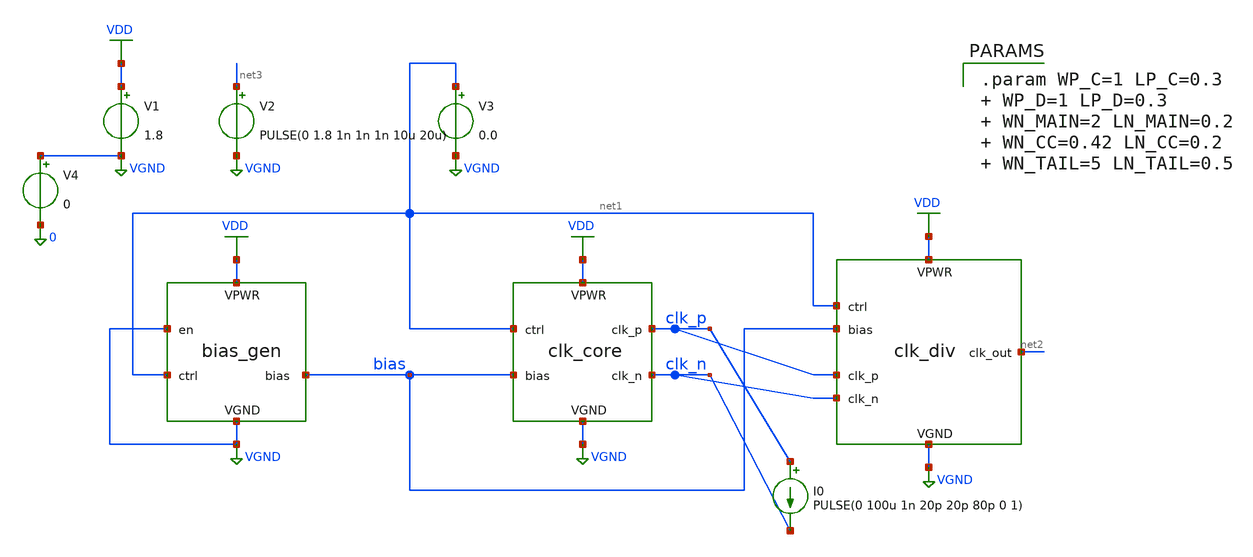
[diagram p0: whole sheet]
** sch_path: simple_vco/v1/tb_proto.sch
**.subckt tb_proto
x1 VDD VGND VGND net1 bias bias_gen
x2 VDD VGND net1 bias clk_p clk_n clk_core
x3 VDD VGND net1 bias clk_p clk_n net2 clk_div
V1 VDD VGND 1.8
V2 net3 VGND PULSE(0 1.8 1n 1n 1n 10u 20u)
V3 net1 VGND 0.0
V4 VGND 0 0
I0 clk_p clk_n PULSE(0 100u 1n 20p 20p 80p 0 1)
**** begin user architecture code


** opencircuitdesign pdks install

.lib $::SKYWATER_MODELS/sky130.lib.spice tt

.include $::SKYWATER_STDCELLS/sky130_fd_sc_hd.spice





.param mc_mm_switch=0
*.option savecurrents
.control

*save all

tran 5p 50n
*plot CLK_OUT CLK_P CLK_N
*plot diff_out
*plot bias

quit 0

.endc

.end




.param WP_C=1 LP_C=0.3  WP_D=1 LP_D=0.3  WN_MAIN=2 LN_MAIN=0.2  WN_CC=0.42 LN_CC=0.2  WN_TAIL=5
+ LN_TAIL=0.5




* 1. Create a continuous differential signal
*B_diff_clk diff_out 0 V=V(clk_p) - V(clk_n)

* 2. Frequency Measurement
* (Wait for the 30th crossing to ensure any startup jitter is gone)
*.meas tran t_start TRIG V(diff_out) VAL=0 RISE=30
*.meas tran t_end   TRIG V(diff_out) VAL=0 RISE=41
*.meas tran period  PARAM='t_end - t_start'
*.meas tran freq    PARAM='1/period'

* 3. Amplitude / Robustness Measurement
* (Measure the peak differential voltage during that exact period)
*.meas tran v_peak MAX V(diff_out) FROM=t_start TO=t_end
*.meas tran v_pp PP V(diff_out) from=30n to=40n


* 1. Create a continuous differential signal
B_diff_clk diff_out 0 V=V(clk_p) - V(clk_n)

* 2. Frequency Measurement
* (Using WHEN to grab exact timestamps)
.meas tran t_start WHEN V(diff_out)=0 RISE=30
.meas tran t_end   WHEN V(diff_out)=0 RISE=41

* (Divide by 11 because RISE 30 to 41 is 11 cycles)
.meas tran period  PARAM='(t_end - t_start) / 11'
.meas tran freq    PARAM='1 / period'

* 3. Amplitude / Robustness Measurement
* (Your static window Peak-to-Peak approach)
.meas tran v_pp PP V(diff_out) FROM=30n TO=40n


**** end user architecture code
**.ends

* expanding   symbol:  bias_gen.sym # of pins=5
** sym_path: simple_vco/v1/bias_gen.sym
** sch_path: simple_vco/v1/bias_gen.sch
.subckt bias_gen VPWR VGND en ctrl bias_out
*.iopin VPWR
*.iopin VGND
*.ipin en
*.ipin ctrl
*.opin bias_out
XM8 net5 net5 VPWR VPWR sky130_fd_pr__pfet_01v8 L=0.3 W=5 nf=1 ad='int((1 + 1)/2) * 5 / 1 * 0.29' as='int((1 + 2)/2) * 5 / 1 * 0.29'
+ pd='2*int((1 + 1)/2) * (5 / 1 + 0.29)' ps='2*int((1 + 2)/2) * (5 / 1 + 0.29)' nrd='0.29 / 5 ' nrs='0.29 / 5 '
+ sa=0 sb=0 sd=0 mult=1 m=1
XM7 bias_out ctrl net3 VPWR sky130_fd_pr__pfet_01v8 L=0.3 W=2 nf=1 ad='int((1 + 1)/2) * 2 / 1 * 0.29'
+ as='int((1 + 2)/2) * 2 / 1 * 0.29' pd='2*int((1 + 1)/2) * (2 / 1 + 0.29)' ps='2*int((1 + 2)/2) * (2 / 1 + 0.29)'
+ nrd='0.29 / 2 ' nrs='0.29 / 2 ' sa=0 sb=0 sd=0 mult=1 m=1
XM6 net4 net1 net3 VPWR sky130_fd_pr__pfet_01v8 L=0.3 W=2 nf=1 ad='int((1 + 1)/2) * 2 / 1 * 0.29' as='int((1 + 2)/2) * 2 / 1 * 0.29'
+ pd='2*int((1 + 1)/2) * (2 / 1 + 0.29)' ps='2*int((1 + 2)/2) * (2 / 1 + 0.29)' nrd='0.29 / 2 ' nrs='0.29 / 2 '
+ sa=0 sb=0 sd=0 mult=1 m=1
XM3 net1 ctrl VPWR VPWR sky130_fd_pr__pfet_01v8 L=LP_C W=WP_C nf=1 ad='int((1 + 1)/2) * WP_C / 1 * 0.29'
+ as='int((1 + 2)/2) * WP_C / 1 * 0.29' pd='2*int((1 + 1)/2) * (WP_C / 1 + 0.29)' ps='2*int((1 + 2)/2) * (WP_C / 1 + 0.29)'
+ nrd='0.29 / WP_C ' nrs='0.29 / WP_C ' sa=0 sb=0 sd=0 mult=1 m=1
XM1 net1 net1 VPWR VPWR sky130_fd_pr__pfet_01v8 L=LP_D W=WP_D nf=1 ad='int((1 + 1)/2) * WP_D / 1 * 0.29'
+ as='int((1 + 2)/2) * WP_D / 1 * 0.29' pd='2*int((1 + 1)/2) * (WP_D / 1 + 0.29)' ps='2*int((1 + 2)/2) * (WP_D / 1 + 0.29)'
+ nrd='0.29 / WP_D ' nrs='0.29 / WP_D ' sa=0 sb=0 sd=0 mult=1 m=1
XM5 net3 net5 VPWR VPWR sky130_fd_pr__pfet_01v8 L=0.3 W=5 nf=1 ad='int((1 + 1)/2) * 5 / 1 * 0.29' as='int((1 + 2)/2) * 5 / 1 * 0.29'
+ pd='2*int((1 + 1)/2) * (5 / 1 + 0.29)' ps='2*int((1 + 2)/2) * (5 / 1 + 0.29)' nrd='0.29 / 5 ' nrs='0.29 / 5 '
+ sa=0 sb=0 sd=0 mult=1 m=1
XM9 bias_out net4 VGND VGND sky130_fd_pr__nfet_01v8 L=0.5 W=5 nf=1 ad='int((1 + 1)/2) * 5 / 1 * 0.29'
+ as='int((1 + 2)/2) * 5 / 1 * 0.29' pd='2*int((1 + 1)/2) * (5 / 1 + 0.29)' ps='2*int((1 + 2)/2) * (5 / 1 + 0.29)'
+ nrd='0.29 / 5 ' nrs='0.29 / 5 ' sa=0 sb=0 sd=0 mult=1 m=1
XM10 net4 net4 VGND VGND sky130_fd_pr__nfet_01v8 L=0.5 W=5 nf=1 ad='int((1 + 1)/2) * 5 / 1 * 0.29' as='int((1 + 2)/2) * 5 / 1 * 0.29'
+ pd='2*int((1 + 1)/2) * (5 / 1 + 0.29)' ps='2*int((1 + 2)/2) * (5 / 1 + 0.29)' nrd='0.29 / 5 ' nrs='0.29 / 5 '
+ sa=0 sb=0 sd=0 mult=1 m=1
XM11 net5 VPWR net6 VGND sky130_fd_pr__nfet_01v8 L=0.2 W=2 nf=1 ad='int((1 + 1)/2) * 2 / 1 * 0.29' as='int((1 + 2)/2) * 2 / 1 * 0.29'
+ pd='2*int((1 + 1)/2) * (2 / 1 + 0.29)' ps='2*int((1 + 2)/2) * (2 / 1 + 0.29)' nrd='0.29 / 2 ' nrs='0.29 / 2 '
+ sa=0 sb=0 sd=0 mult=1 m=1
XM12 net6 bias_out VGND VGND sky130_fd_pr__nfet_01v8 L=0.5 W=5 nf=1 ad='int((1 + 1)/2) * 5 / 1 * 0.29'
+ as='int((1 + 2)/2) * 5 / 1 * 0.29' pd='2*int((1 + 1)/2) * (5 / 1 + 0.29)' ps='2*int((1 + 2)/2) * (5 / 1 + 0.29)'
+ nrd='0.29 / 5 ' nrs='0.29 / 5 ' sa=0 sb=0 sd=0 mult=1 m=1
XM13 net6 net7 VGND VGND sky130_fd_pr__nfet_01v8 L=0.15 W=5 nf=1 ad='int((1 + 1)/2) * 5 / 1 * 0.29' as='int((1 + 2)/2) * 5 / 1 * 0.29'
+ pd='2*int((1 + 1)/2) * (5 / 1 + 0.29)' ps='2*int((1 + 2)/2) * (5 / 1 + 0.29)' nrd='0.29 / 5 ' nrs='0.29 / 5 '
+ sa=0 sb=0 sd=0 mult=1 m=1
XM14 net7 net8 VPWR VPWR sky130_fd_pr__pfet_01v8 L=0.15 W=1 nf=1 ad='int((1 + 1)/2) * 1 / 1 * 0.29' as='int((1 + 2)/2) * 1 / 1 * 0.29'
+ pd='2*int((1 + 1)/2) * (1 / 1 + 0.29)' ps='2*int((1 + 2)/2) * (1 / 1 + 0.29)' nrd='0.29 / 1 ' nrs='0.29 / 1 '
+ sa=0 sb=0 sd=0 mult=1 m=1
XM15 net7 net8 VGND VGND sky130_fd_pr__nfet_01v8 L=0.15 W=1 nf=1 ad='int((1 + 1)/2) * 1 / 1 * 0.29' as='int((1 + 2)/2) * 1 / 1 * 0.29'
+ pd='2*int((1 + 1)/2) * (1 / 1 + 0.29)' ps='2*int((1 + 2)/2) * (1 / 1 + 0.29)' nrd='0.29 / 1 ' nrs='0.29 / 1 '
+ sa=0 sb=0 sd=0 mult=1 m=1
XM16 net8 net9 VPWR VPWR sky130_fd_pr__pfet_01v8 L=0.15 W=1 nf=1 ad='int((1 + 1)/2) * 1 / 1 * 0.29' as='int((1 + 2)/2) * 1 / 1 * 0.29'
+ pd='2*int((1 + 1)/2) * (1 / 1 + 0.29)' ps='2*int((1 + 2)/2) * (1 / 1 + 0.29)' nrd='0.29 / 1 ' nrs='0.29 / 1 '
+ sa=0 sb=0 sd=0 mult=1 m=1
XM17 net8 net9 VGND VGND sky130_fd_pr__nfet_01v8 L=0.15 W=1 nf=1 ad='int((1 + 1)/2) * 1 / 1 * 0.29' as='int((1 + 2)/2) * 1 / 1 * 0.29'
+ pd='2*int((1 + 1)/2) * (1 / 1 + 0.29)' ps='2*int((1 + 2)/2) * (1 / 1 + 0.29)' nrd='0.29 / 1 ' nrs='0.29 / 1 '
+ sa=0 sb=0 sd=0 mult=1 m=1
XM19 net9 bias_out VGND VGND sky130_fd_pr__nfet_01v8 L=0.15 W=1 nf=1 ad='int((1 + 1)/2) * 1 / 1 * 0.29'
+ as='int((1 + 2)/2) * 1 / 1 * 0.29' pd='2*int((1 + 1)/2) * (1 / 1 + 0.29)' ps='2*int((1 + 2)/2) * (1 / 1 + 0.29)'
+ nrd='0.29 / 1 ' nrs='0.29 / 1 ' sa=0 sb=0 sd=0 mult=1 m=1
XM18 net9 en VPWR VPWR sky130_fd_pr__pfet_01v8_hvt L=8 W=0.42 nf=1 ad='int((1 + 1)/2) * 0.42 / 1 * 0.29'
+ as='int((1 + 2)/2) * 0.42 / 1 * 0.29' pd='2*int((1 + 1)/2) * (0.42 / 1 + 0.29)' ps='2*int((1 + 2)/2) * (0.42 / 1 + 0.29)'
+ nrd='0.29 / 0.42 ' nrs='0.29 / 0.42 ' sa=0 sb=0 sd=0 mult=1 m=1
XM20 bias_out en VGND VGND sky130_fd_pr__nfet_01v8 L=0.15 W=0.42 nf=1 ad='int((1 + 1)/2) * 0.42 / 1 * 0.29'
+ as='int((1 + 2)/2) * 0.42 / 1 * 0.29' pd='2*int((1 + 1)/2) * (0.42 / 1 + 0.29)' ps='2*int((1 + 2)/2) * (0.42 / 1 + 0.29)'
+ nrd='0.29 / 0.42 ' nrs='0.29 / 0.42 ' sa=0 sb=0 sd=0 mult=1 m=1
XM21 net9 en VGND VGND sky130_fd_pr__nfet_01v8 L=0.15 W=0.42 nf=1 ad='int((1 + 1)/2) * 0.42 / 1 * 0.29'
+ as='int((1 + 2)/2) * 0.42 / 1 * 0.29' pd='2*int((1 + 1)/2) * (0.42 / 1 + 0.29)' ps='2*int((1 + 2)/2) * (0.42 / 1 + 0.29)'
+ nrd='0.29 / 0.42 ' nrs='0.29 / 0.42 ' sa=0 sb=0 sd=0 mult=1 m=1
XM4 net2 bias_out VGND VGND sky130_fd_pr__nfet_01v8 L=LN_TAIL W=WN_TAIL nf=1 ad='int((1 + 1)/2) * WN_TAIL / 1 * 0.29'
+ as='int((1 + 2)/2) * WN_TAIL / 1 * 0.29' pd='2*int((1 + 1)/2) * (WN_TAIL / 1 + 0.29)' ps='2*int((1 + 2)/2) * (WN_TAIL / 1 + 0.29)'
+ nrd='0.29 / WN_TAIL ' nrs='0.29 / WN_TAIL ' sa=0 sb=0 sd=0 mult=1 m=1
XM2 net1 VPWR net2 VGND sky130_fd_pr__nfet_01v8 L=LN_MAIN W=WN_MAIN nf=1 ad='int((1 + 1)/2) * WN_MAIN / 1 * 0.29'
+ as='int((1 + 2)/2) * WN_MAIN / 1 * 0.29' pd='2*int((1 + 1)/2) * (WN_MAIN / 1 + 0.29)' ps='2*int((1 + 2)/2) * (WN_MAIN / 1 + 0.29)'
+ nrd='0.29 / WN_MAIN ' nrs='0.29 / WN_MAIN ' sa=0 sb=0 sd=0 mult=1 m=1
.ends


* expanding   symbol:  clk_core.sym # of pins=6
** sym_path: simple_vco/v1/clk_core.sym
** sch_path: simple_vco/v1/clk_core.sch
.subckt clk_core VPWR VGND ctrl bias_in clk_p clk_n
*.iopin VPWR
*.iopin VGND
*.ipin ctrl
*.ipin bias_in
*.opin clk_p
*.opin clk_n
XM3 clk_p ctrl VPWR VPWR sky130_fd_pr__pfet_01v8 L=LP_C W=WP_C nf=1 ad='int((1 + 1)/2) * WP_C / 1 * 0.29'
+ as='int((1 + 2)/2) * WP_C / 1 * 0.29' pd='2*int((1 + 1)/2) * (WP_C / 1 + 0.29)' ps='2*int((1 + 2)/2) * (WP_C / 1 + 0.29)'
+ nrd='0.29 / WP_C ' nrs='0.29 / WP_C ' sa=0 sb=0 sd=0 mult=1 m=1
XM1 clk_p clk_p VPWR VPWR sky130_fd_pr__pfet_01v8 L=LP_D W=WP_D nf=1 ad='int((1 + 1)/2) * WP_D / 1 * 0.29'
+ as='int((1 + 2)/2) * WP_D / 1 * 0.29' pd='2*int((1 + 1)/2) * (WP_D / 1 + 0.29)' ps='2*int((1 + 2)/2) * (WP_D / 1 + 0.29)'
+ nrd='0.29 / WP_D ' nrs='0.29 / WP_D ' sa=0 sb=0 sd=0 mult=1 m=1
XM4 net1 bias_in VGND VGND sky130_fd_pr__nfet_01v8 L=LN_TAIL W=WN_TAIL nf=1 ad='int((1 + 1)/2) * WN_TAIL / 1 * 0.29'
+ as='int((1 + 2)/2) * WN_TAIL / 1 * 0.29' pd='2*int((1 + 1)/2) * (WN_TAIL / 1 + 0.29)' ps='2*int((1 + 2)/2) * (WN_TAIL / 1 + 0.29)'
+ nrd='0.29 / WN_TAIL ' nrs='0.29 / WN_TAIL ' sa=0 sb=0 sd=0 mult=1 m=1
XM2 clk_p clk_2_p net1 VGND sky130_fd_pr__nfet_01v8 L=LN_MAIN W=WN_MAIN nf=1 ad='int((1 + 1)/2) * WN_MAIN / 1 * 0.29'
+ as='int((1 + 2)/2) * WN_MAIN / 1 * 0.29' pd='2*int((1 + 1)/2) * (WN_MAIN / 1 + 0.29)' ps='2*int((1 + 2)/2) * (WN_MAIN / 1 + 0.29)'
+ nrd='0.29 / WN_MAIN ' nrs='0.29 / WN_MAIN ' sa=0 sb=0 sd=0 mult=1 m=1
XM5 clk_n ctrl VPWR VPWR sky130_fd_pr__pfet_01v8 L=LP_C W=WP_C nf=1 ad='int((1 + 1)/2) * WP_C / 1 * 0.29'
+ as='int((1 + 2)/2) * WP_C / 1 * 0.29' pd='2*int((1 + 1)/2) * (WP_C / 1 + 0.29)' ps='2*int((1 + 2)/2) * (WP_C / 1 + 0.29)'
+ nrd='0.29 / WP_C ' nrs='0.29 / WP_C ' sa=0 sb=0 sd=0 mult=1 m=1
XM6 clk_n clk_n VPWR VPWR sky130_fd_pr__pfet_01v8 L=LP_D W=WP_D nf=1 ad='int((1 + 1)/2) * WP_D / 1 * 0.29'
+ as='int((1 + 2)/2) * WP_D / 1 * 0.29' pd='2*int((1 + 1)/2) * (WP_D / 1 + 0.29)' ps='2*int((1 + 2)/2) * (WP_D / 1 + 0.29)'
+ nrd='0.29 / WP_D ' nrs='0.29 / WP_D ' sa=0 sb=0 sd=0 mult=1 m=1
XM8 clk_n clk_2_n net1 VGND sky130_fd_pr__nfet_01v8 L=LN_MAIN W=WN_MAIN nf=1 ad='int((1 + 1)/2) * WN_MAIN / 1 * 0.29'
+ as='int((1 + 2)/2) * WN_MAIN / 1 * 0.29' pd='2*int((1 + 1)/2) * (WN_MAIN / 1 + 0.29)' ps='2*int((1 + 2)/2) * (WN_MAIN / 1 + 0.29)'
+ nrd='0.29 / WN_MAIN ' nrs='0.29 / WN_MAIN ' sa=0 sb=0 sd=0 mult=1 m=1
XM7 clk_n clk_p net1 VGND sky130_fd_pr__nfet_01v8 L=LN_CC W=WN_CC nf=1 ad='int((1 + 1)/2) * WN_CC / 1 * 0.29'
+ as='int((1 + 2)/2) * WN_CC / 1 * 0.29' pd='2*int((1 + 1)/2) * (WN_CC / 1 + 0.29)' ps='2*int((1 + 2)/2) * (WN_CC / 1 + 0.29)'
+ nrd='0.29 / WN_CC ' nrs='0.29 / WN_CC ' sa=0 sb=0 sd=0 mult=1 m=1
XM9 clk_p clk_n net1 VGND sky130_fd_pr__nfet_01v8 L=LN_CC W=WN_CC nf=1 ad='int((1 + 1)/2) * WN_CC / 1 * 0.29'
+ as='int((1 + 2)/2) * WN_CC / 1 * 0.29' pd='2*int((1 + 1)/2) * (WN_CC / 1 + 0.29)' ps='2*int((1 + 2)/2) * (WN_CC / 1 + 0.29)'
+ nrd='0.29 / WN_CC ' nrs='0.29 / WN_CC ' sa=0 sb=0 sd=0 mult=1 m=1
XM10 clk_2_n ctrl VPWR VPWR sky130_fd_pr__pfet_01v8 L=LP_C W=WP_C nf=1 ad='int((1 + 1)/2) * WP_C / 1 * 0.29'
+ as='int((1 + 2)/2) * WP_C / 1 * 0.29' pd='2*int((1 + 1)/2) * (WP_C / 1 + 0.29)' ps='2*int((1 + 2)/2) * (WP_C / 1 + 0.29)'
+ nrd='0.29 / WP_C ' nrs='0.29 / WP_C ' sa=0 sb=0 sd=0 mult=1 m=1
XM11 clk_2_n clk_2_n VPWR VPWR sky130_fd_pr__pfet_01v8 L=LP_D W=WP_D nf=1 ad='int((1 + 1)/2) * WP_D / 1 * 0.29'
+ as='int((1 + 2)/2) * WP_D / 1 * 0.29' pd='2*int((1 + 1)/2) * (WP_D / 1 + 0.29)' ps='2*int((1 + 2)/2) * (WP_D / 1 + 0.29)'
+ nrd='0.29 / WP_D ' nrs='0.29 / WP_D ' sa=0 sb=0 sd=0 mult=1 m=1
XM12 net2 bias_in VGND VGND sky130_fd_pr__nfet_01v8 L=LN_TAIL W=WN_TAIL nf=1 ad='int((1 + 1)/2) * WN_TAIL / 1 * 0.29'
+ as='int((1 + 2)/2) * WN_TAIL / 1 * 0.29' pd='2*int((1 + 1)/2) * (WN_TAIL / 1 + 0.29)' ps='2*int((1 + 2)/2) * (WN_TAIL / 1 + 0.29)'
+ nrd='0.29 / WN_TAIL ' nrs='0.29 / WN_TAIL ' sa=0 sb=0 sd=0 mult=1 m=1
XM13 clk_2_n clk_p net2 VGND sky130_fd_pr__nfet_01v8 L=LN_MAIN W=WN_MAIN nf=1 ad='int((1 + 1)/2) * WN_MAIN / 1 * 0.29'
+ as='int((1 + 2)/2) * WN_MAIN / 1 * 0.29' pd='2*int((1 + 1)/2) * (WN_MAIN / 1 + 0.29)' ps='2*int((1 + 2)/2) * (WN_MAIN / 1 + 0.29)'
+ nrd='0.29 / WN_MAIN ' nrs='0.29 / WN_MAIN ' sa=0 sb=0 sd=0 mult=1 m=1
XM14 clk_2_p ctrl VPWR VPWR sky130_fd_pr__pfet_01v8 L=LP_C W=WP_C nf=1 ad='int((1 + 1)/2) * WP_C / 1 * 0.29'
+ as='int((1 + 2)/2) * WP_C / 1 * 0.29' pd='2*int((1 + 1)/2) * (WP_C / 1 + 0.29)' ps='2*int((1 + 2)/2) * (WP_C / 1 + 0.29)'
+ nrd='0.29 / WP_C ' nrs='0.29 / WP_C ' sa=0 sb=0 sd=0 mult=1 m=1
XM15 clk_2_p clk_2_p VPWR VPWR sky130_fd_pr__pfet_01v8 L=LP_D W=WP_D nf=1 ad='int((1 + 1)/2) * WP_D / 1 * 0.29'
+ as='int((1 + 2)/2) * WP_D / 1 * 0.29' pd='2*int((1 + 1)/2) * (WP_D / 1 + 0.29)' ps='2*int((1 + 2)/2) * (WP_D / 1 + 0.29)'
+ nrd='0.29 / WP_D ' nrs='0.29 / WP_D ' sa=0 sb=0 sd=0 mult=1 m=1
XM16 clk_2_p clk_n net2 VGND sky130_fd_pr__nfet_01v8 L=LN_MAIN W=WN_MAIN nf=1 ad='int((1 + 1)/2) * WN_MAIN / 1 * 0.29'
+ as='int((1 + 2)/2) * WN_MAIN / 1 * 0.29' pd='2*int((1 + 1)/2) * (WN_MAIN / 1 + 0.29)' ps='2*int((1 + 2)/2) * (WN_MAIN / 1 + 0.29)'
+ nrd='0.29 / WN_MAIN ' nrs='0.29 / WN_MAIN ' sa=0 sb=0 sd=0 mult=1 m=1
XM17 clk_2_p clk_2_n net2 VGND sky130_fd_pr__nfet_01v8 L=LN_CC W=WN_CC nf=1 ad='int((1 + 1)/2) * WN_CC / 1 * 0.29'
+ as='int((1 + 2)/2) * WN_CC / 1 * 0.29' pd='2*int((1 + 1)/2) * (WN_CC / 1 + 0.29)' ps='2*int((1 + 2)/2) * (WN_CC / 1 + 0.29)'
+ nrd='0.29 / WN_CC ' nrs='0.29 / WN_CC ' sa=0 sb=0 sd=0 mult=1 m=1
XM18 clk_2_n clk_2_p net2 VGND sky130_fd_pr__nfet_01v8 L=LN_CC W=WN_CC nf=1 ad='int((1 + 1)/2) * WN_CC / 1 * 0.29'
+ as='int((1 + 2)/2) * WN_CC / 1 * 0.29' pd='2*int((1 + 1)/2) * (WN_CC / 1 + 0.29)' ps='2*int((1 + 2)/2) * (WN_CC / 1 + 0.29)'
+ nrd='0.29 / WN_CC ' nrs='0.29 / WN_CC ' sa=0 sb=0 sd=0 mult=1 m=1
.ends


* expanding   symbol:  clk_div.sym # of pins=7
** sym_path: simple_vco/v1/clk_div.sym
** sch_path: simple_vco/v1/clk_div.sch
.subckt clk_div VPWR VGND ctrl bias_in clk_p clk_n clk_out
*.iopin VPWR
*.iopin VGND
*.ipin ctrl
*.ipin bias_in
*.ipin clk_p
*.ipin clk_n
*.opin clk_out
.ends

.GLOBAL VGND
.GLOBAL VDD
.end
